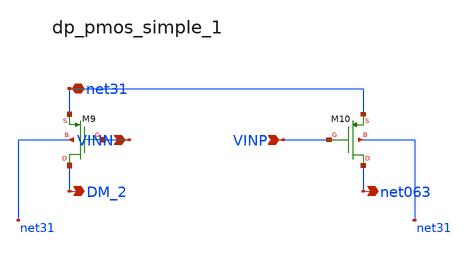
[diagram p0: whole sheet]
** sch_path: analog-db/raw/amp_006_leung_dfcfc1/hier/blocks/dp_pmos_simple_1.sch
**.subckt dp_pmos_simple_1 VINN VINP net31 DM_2 net063
*.ipin VINN
*.ipin VINP
*.iopin net31
*.opin DM_2
*.opin net063
XM10 net063 VINP net31 net31 sg13_lv_pmos w=x_dut_xm10_w l=x_dut_xm10_l ng=1 m=x_dut_xm10_m
XM9 DM_2 VINN net31 net31 sg13_lv_pmos w=x_dut_xm9_w l=x_dut_xm9_l ng=1 m=x_dut_xm9_m
**.ends
.end
